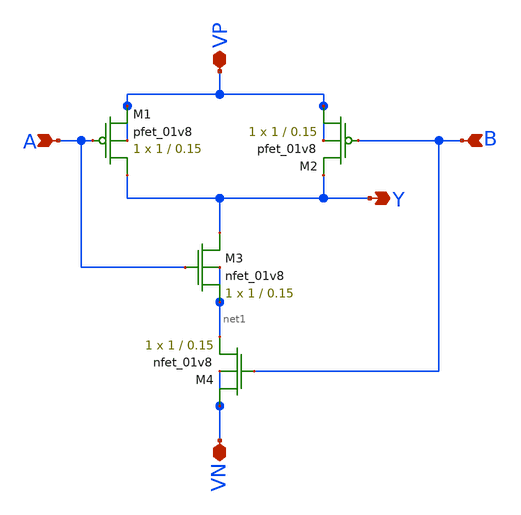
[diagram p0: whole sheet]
** sch_path: mini_proj_1/schematic/nand.sch
**.subckt nand A B VP VN Y
*.ipin A
*.ipin B
*.iopin VP
*.iopin VN
*.opin Y
XM1 Y A VP VP sky130_fd_pr__pfet_01v8 L=0.15 W=1 nf=1 ad='int((nf+1)/2) * W/nf * 0.29' as='int((nf+2)/2) * W/nf * 0.29'
+ pd='2*int((nf+1)/2) * (W/nf + 0.29)' ps='2*int((nf+2)/2) * (W/nf + 0.29)' nrd='0.29 / W' nrs='0.29 / W'
+ sa=0 sb=0 sd=0 mult=1 m=1
XM2 VP B Y VP sky130_fd_pr__pfet_01v8 L=0.15 W=1 nf=1 ad='int((nf+1)/2) * W/nf * 0.29' as='int((nf+2)/2) * W/nf * 0.29'
+ pd='2*int((nf+1)/2) * (W/nf + 0.29)' ps='2*int((nf+2)/2) * (W/nf + 0.29)' nrd='0.29 / W' nrs='0.29 / W'
+ sa=0 sb=0 sd=0 mult=1 m=1
XM3 Y A net1 net1 sky130_fd_pr__nfet_01v8 L=0.15 W=1 nf=1 ad='int((nf+1)/2) * W/nf * 0.29' as='int((nf+2)/2) * W/nf * 0.29'
+ pd='2*int((nf+1)/2) * (W/nf + 0.29)' ps='2*int((nf+2)/2) * (W/nf + 0.29)' nrd='0.29 / W' nrs='0.29 / W'
+ sa=0 sb=0 sd=0 mult=1 m=1
XM4 VN B net1 VN sky130_fd_pr__nfet_01v8 L=0.15 W=1 nf=1 ad='int((nf+1)/2) * W/nf * 0.29' as='int((nf+2)/2) * W/nf * 0.29'
+ pd='2*int((nf+1)/2) * (W/nf + 0.29)' ps='2*int((nf+2)/2) * (W/nf + 0.29)' nrd='0.29 / W' nrs='0.29 / W'
+ sa=0 sb=0 sd=0 mult=1 m=1
**.ends
.end
